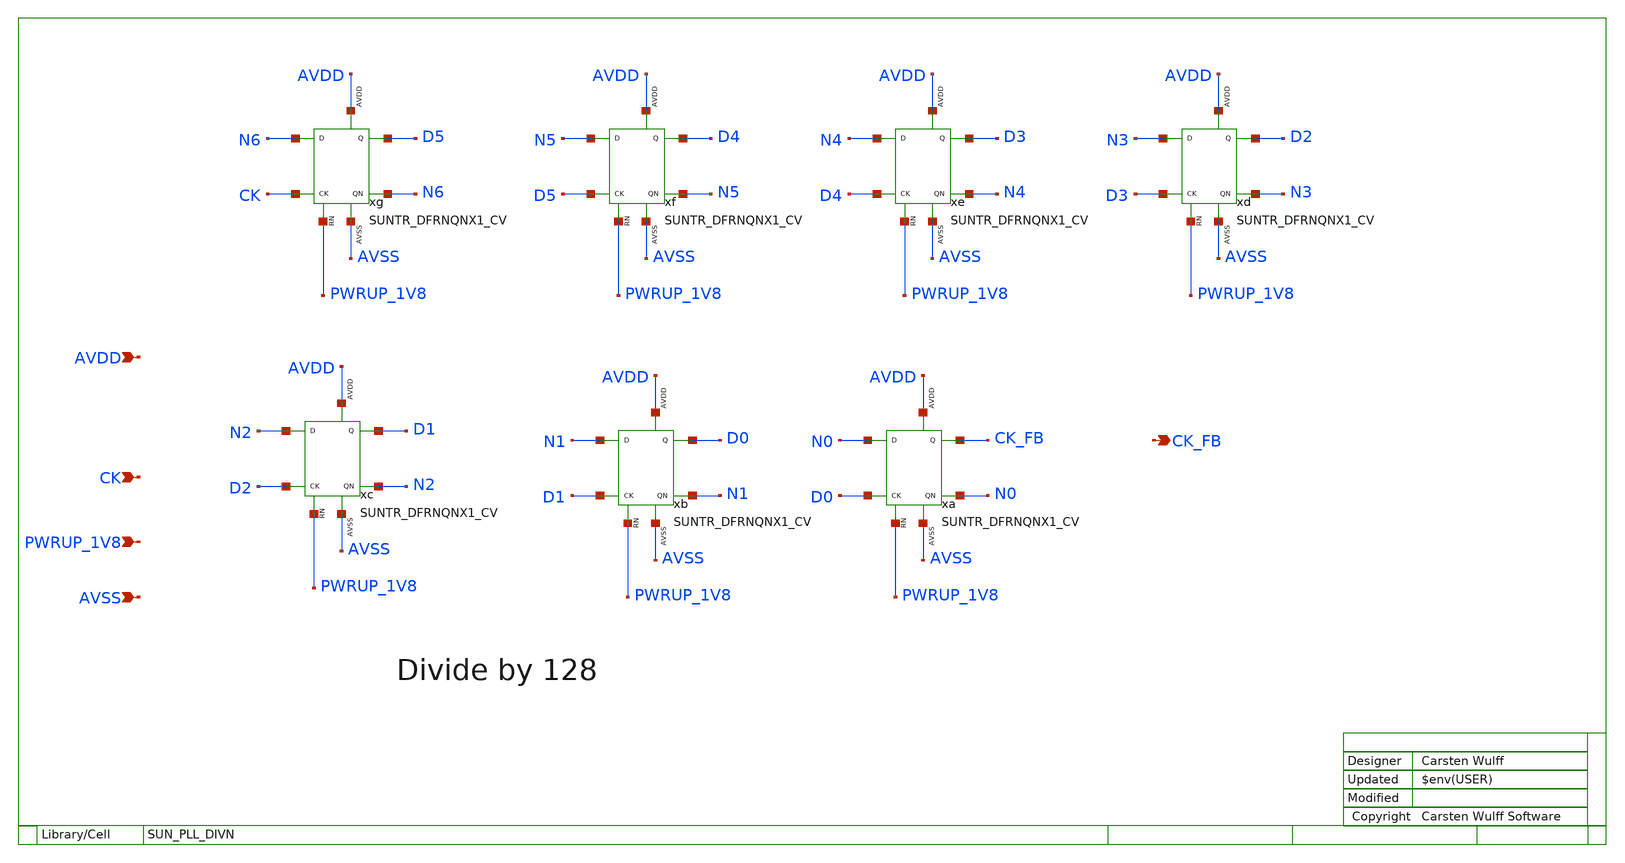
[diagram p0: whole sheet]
** sch_path: ip/sun_pll_sky130nm/design/SUN_PLL_SKY130NM/SUN_PLL_DIVN.sch
**.subckt SUN_PLL_DIVN PWRUP_1V8 CK AVDD AVSS CK_FB
*.ipin PWRUP_1V8
*.ipin CK
*.ipin AVDD
*.ipin AVSS
*.opin CK_FB
xg N6 CK PWRUP_1V8 D5 N6 AVDD AVSS SUNTR_DFRNQNX1_CV
xf N5 D5 PWRUP_1V8 D4 N5 AVDD AVSS SUNTR_DFRNQNX1_CV
xe N4 D4 PWRUP_1V8 D3 N4 AVDD AVSS SUNTR_DFRNQNX1_CV
xd N3 D3 PWRUP_1V8 D2 N3 AVDD AVSS SUNTR_DFRNQNX1_CV
xc N2 D2 PWRUP_1V8 D1 N2 AVDD AVSS SUNTR_DFRNQNX1_CV
xb N1 D1 PWRUP_1V8 D0 N1 AVDD AVSS SUNTR_DFRNQNX1_CV
xa N0 D0 PWRUP_1V8 CK_FB N0 AVDD AVSS SUNTR_DFRNQNX1_CV
**.ends
.end
